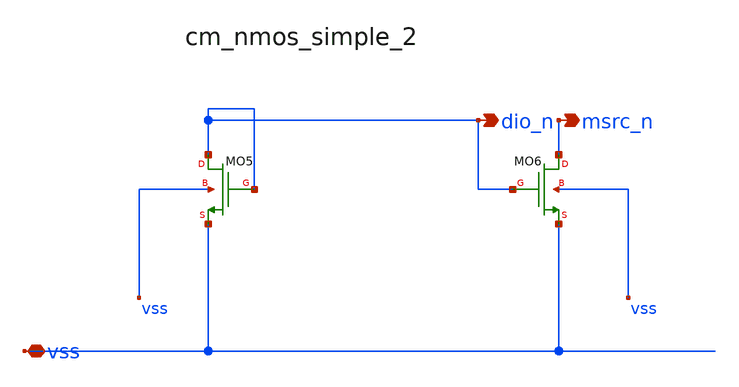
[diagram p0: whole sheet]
** sch_path: analog-db/raw/ia_001_hsu_bandpass_classab/hier/blocks/cm_nmos_simple_2.sch
**.subckt cm_nmos_simple_2 vss dio_n msrc_n
*.iopin vss
*.opin dio_n
*.opin msrc_n
XMO5 dio_n dio_n vss vss sg13_lv_nmos w=x_dut_xmo5_w l=x_dut_xmo5_l ng=1 m=x_dut_xmo5_m
XMO6 msrc_n dio_n vss vss sg13_lv_nmos w=x_dut_xmo6_w l=x_dut_xmo6_l ng=1 m=x_dut_xmo6_m
**.ends
.end
